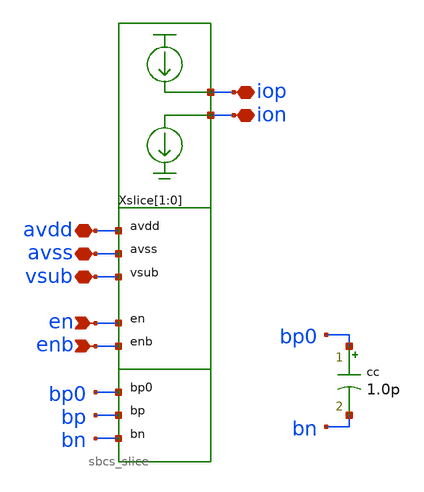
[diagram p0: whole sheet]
** sch_path: xschem/sbcs.sch
**.subckt sbcs avdd avss iop ion vsub en enb
*.iopin avdd
*.iopin avss
*.iopin iop
*.iopin ion
*.iopin vsub
*.ipin en
*.ipin enb
Xslice[1] iop ion avdd avss en enb bp0 bp bn sbcs_slice
Xslice[0] iop ion avdd avss en enb bp0 bp bn sbcs_slice
cc bp0 bn 1.0p m=1
**.ends
.end
